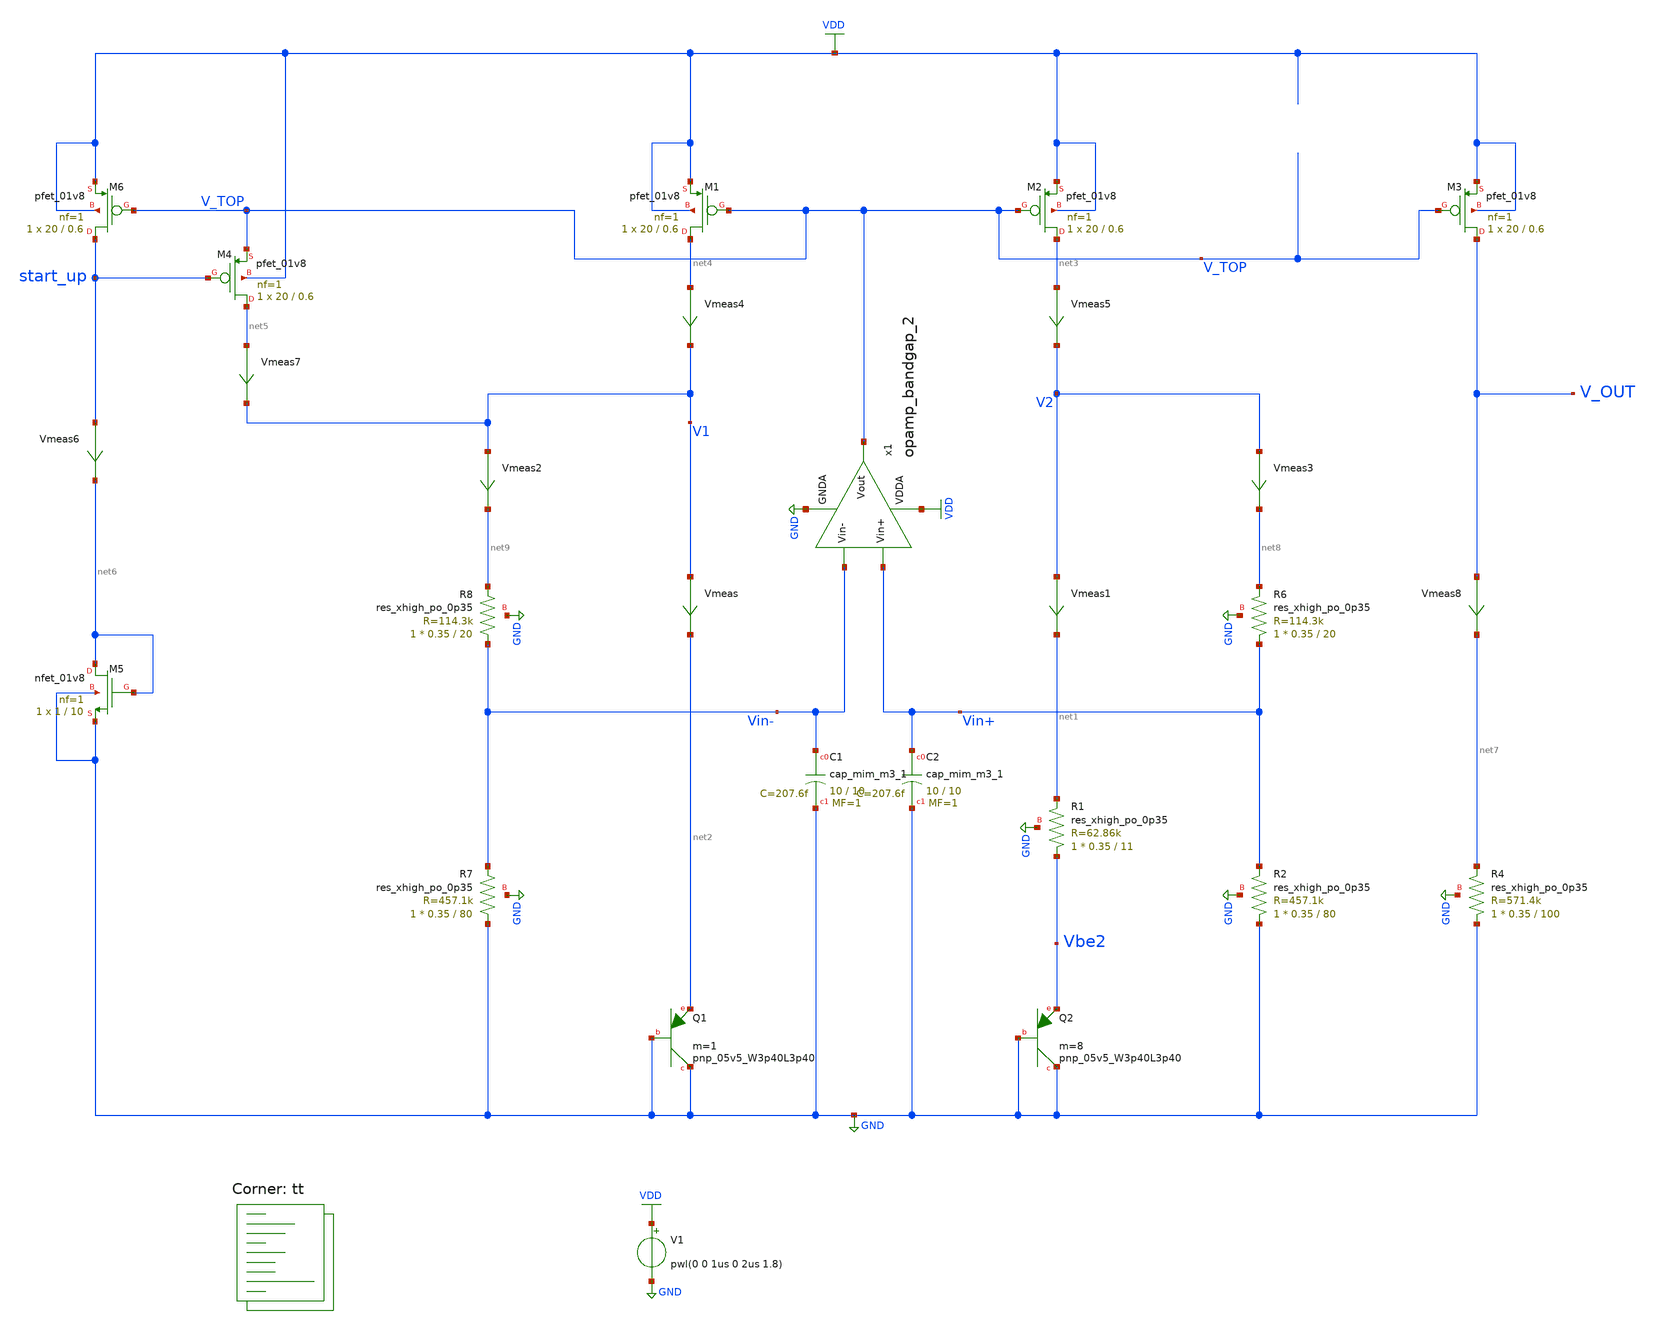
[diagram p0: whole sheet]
** sch_path: projects/bandgapref/xschem_ngspice/new_files/tb_low_voltage_BGR_9.sch
**.subckt tb_low_voltage_BGR_9
V1 VDD GND pwl(0 0 1us 0 2us 1.8)
XQ1 GND GND net2 sky130_fd_pr__pnp_05v5_W3p40L3p40 m=1
XQ2 GND GND Vbe2 sky130_fd_pr__pnp_05v5_W3p40L3p40 m=8
XM1 net4 V_TOP VDD VDD sky130_fd_pr__pfet_01v8 L=0.6 W=20 nf=1 ad='int((nf+1)/2) * W/nf * 0.29' as='int((nf+2)/2) * W/nf * 0.29'
+ pd='2*int((nf+1)/2) * (W/nf + 0.29)' ps='2*int((nf+2)/2) * (W/nf + 0.29)' nrd='0.29 / W' nrs='0.29 / W'
+ sa=0 sb=0 sd=0 mult=1 m=1
XM2 net3 V_TOP VDD VDD sky130_fd_pr__pfet_01v8 L=0.6 W=20 nf=1 ad='int((nf+1)/2) * W/nf * 0.29' as='int((nf+2)/2) * W/nf * 0.29'
+ pd='2*int((nf+1)/2) * (W/nf + 0.29)' ps='2*int((nf+2)/2) * (W/nf + 0.29)' nrd='0.29 / W' nrs='0.29 / W'
+ sa=0 sb=0 sd=0 mult=1 m=1
XM3 V_OUT V_TOP VDD VDD sky130_fd_pr__pfet_01v8 L=0.6 W=20 nf=1 ad='int((nf+1)/2) * W/nf * 0.29' as='int((nf+2)/2) * W/nf * 0.29'
+ pd='2*int((nf+1)/2) * (W/nf + 0.29)' ps='2*int((nf+2)/2) * (W/nf + 0.29)' nrd='0.29 / W' nrs='0.29 / W'
+ sa=0 sb=0 sd=0 mult=1 m=1
Vmeas V1 net2 0
.save i(vmeas)
Vmeas1 V2 net1 0
.save i(vmeas1)
Vmeas2 V1 net9 0
.save i(vmeas2)
XR1 Vbe2 net1 GND sky130_fd_pr__res_xhigh_po_0p35 L=11 mult=1 m=1
XR2 GND Vin+ GND sky130_fd_pr__res_xhigh_po_0p35 L=80 mult=1 m=1
XR4 GND net7 GND sky130_fd_pr__res_xhigh_po_0p35 L=100 mult=1 m=1
Vmeas3 V2 net8 0
.save i(vmeas3)
Vmeas4 net4 V1 0
.save i(vmeas4)
XM5 net6 net6 GND GND sky130_fd_pr__nfet_01v8 L=10 W=1 nf=1 ad='int((nf+1)/2) * W/nf * 0.29' as='int((nf+2)/2) * W/nf * 0.29'
+ pd='2*int((nf+1)/2) * (W/nf + 0.29)' ps='2*int((nf+2)/2) * (W/nf + 0.29)' nrd='0.29 / W' nrs='0.29 / W'
+ sa=0 sb=0 sd=0 mult=1 m=1
XM6 start_up V_TOP VDD VDD sky130_fd_pr__pfet_01v8 L=0.6 W=20 nf=1 ad='int((nf+1)/2) * W/nf * 0.29' as='int((nf+2)/2) * W/nf * 0.29'
+ pd='2*int((nf+1)/2) * (W/nf + 0.29)' ps='2*int((nf+2)/2) * (W/nf + 0.29)' nrd='0.29 / W' nrs='0.29 / W'
+ sa=0 sb=0 sd=0 mult=1 m=1
Vmeas5 net3 V2 0
.save i(vmeas5)
XM4 net5 start_up V_TOP VDD sky130_fd_pr__pfet_01v8 L=0.6 W=20 nf=1 ad='int((nf+1)/2) * W/nf * 0.29'
+ as='int((nf+2)/2) * W/nf * 0.29' pd='2*int((nf+1)/2) * (W/nf + 0.29)' ps='2*int((nf+2)/2) * (W/nf + 0.29)'
+ nrd='0.29 / W' nrs='0.29 / W' sa=0 sb=0 sd=0 mult=1 m=1
Vmeas7 net5 V1 0
.save i(vmeas7)
x1 VDD V_TOP Vin- Vin+ GND opamp_bandgap_2
XR6 Vin+ net8 GND sky130_fd_pr__res_xhigh_po_0p35 L=20 mult=1 m=1
XR7 GND Vin- GND sky130_fd_pr__res_xhigh_po_0p35 L=80 mult=1 m=1
Vmeas8 V_OUT net7 0
.save i(vmeas8)
XR8 Vin- net9 GND sky130_fd_pr__res_xhigh_po_0p35 L=20 mult=1 m=1
Vmeas6 start_up net6 0
.save i(vmeas6)
XC1 Vin- GND sky130_fd_pr__cap_mim_m3_1 W=10 L=10 MF=1 m=1
XC2 Vin+ GND sky130_fd_pr__cap_mim_m3_1 W=10 L=10 MF=1 m=1
**** begin user architecture code
.lib $::SKYWATER_MODELS/sky130.lib.spice tt



.option method=gear
.option wnflag=1
.option savecurrents
* .temp =140

.save @m.xm1.msky130_fd_pr__pfet_01v8[gm] @m.xm1.msky130_fd_pr__pfet_01v8[vth] @m.xm1.msky130_fd_pr__pfet_01v8[vgs] @m.xm1.msky130_fd_pr__pfet_01v8[vds] @m.xm2.msky130_fd_pr__pfet_01v8[gm] @m.xm2.msky130_fd_pr__pfet_01v8[vth] @m.xm2.msky130_fd_pr__pfet_01v8[vgs] @m.xm2.msky130_fd_pr__pfet_01v8[vds] @m.xm3.msky130_fd_pr__pfet_01v8[gm] @m.xm4.msky130_fd_pr__pfet_01v8[gm] @m.xm4.msky130_fd_pr__nfet_01v8[gm] @m.x1.xm1.msky130_fd_pr__nfet_01v8[gm] @m.x1.xm2.msky130_fd_pr__nfet_01v8[gm] @m.x1.xm3.msky130_fd_pr__nfet_01v8[gm] @m.x1.xm4.msky130_fd_pr__pfet_01v8[gm] @m.x1.xm5.msky130_fd_pr__pfet_01v8[gm] @m.x1.xm6.msky130_fd_pr__nfet_01v8[gm] @m.x1.xm7.msky130_fd_pr__pfet_01v8[gm] @m.x2.xm1.msky130_fd_pr__nfet_01v8[gm] @m.x2.xm2.msky130_fd_pr__nfet_01v8[gm] @m.x2.xm3.msky130_fd_pr__nfet_01v8[gm] @m.x2.xm4.msky130_fd_pr__pfet_01v8[gm] @m.x2.xm5.msky130_fd_pr__pfet_01v8[gm] @m.x2.xm6.msky130_fd_pr__pfet_01v8[gm] @m.x2.xm7.msky130_fd_pr__pfet_01v8[gm]

* .ic v(vin-) = 0.8
* .ic v(vin+) = 0.8
* .ic v(v_top) = 1.8

.control

    save all
    * dc temp -40 120 5 V1 1.6 2.0 0.05
    * dc V1 1.7 1.9 0.001 temp -40 120 40
    * dc V1 0.0 2.0 0.02 temp -40 120 40
    * dc V1 0 2.0 0.02
    tran 1ns 8us
    remzerovec
    * write tb_low_voltage_BGR_9.raw
    write tb_low_voltage_BGR_9_2.raw

.endc



**** end user architecture code
**.ends

* expanding   symbol:  opamp_bandgap_2.sym # of pins=5
** sym_path: projects/bandgapref/xschem_ngspice/new_files/opamp_bandgap_2.sym
** sch_path: projects/bandgapref/xschem_ngspice/new_files/opamp_bandgap_2.sch
.subckt opamp_bandgap_2 VDDA Vout Vin- Vin+ GNDA
*.ipin Vin+
*.opin Vout
*.ipin Vin-
*.ipin GNDA
*.ipin VDDA
XM1 V_p V_mirror GNDA GNDA sky130_fd_pr__nfet_01v8 L=10 W=10 nf=1 ad='int((nf+1)/2) * W/nf * 0.29' as='int((nf+2)/2) * W/nf * 0.29'
+ pd='2*int((nf+1)/2) * (W/nf + 0.29)' ps='2*int((nf+2)/2) * (W/nf + 0.29)' nrd='0.29 / W' nrs='0.29 / W'
+ sa=0 sb=0 sd=0 mult=1 m=1
XM2 V_mirror Vin- V_p GNDA sky130_fd_pr__nfet_01v8 L=1.2 W=10 nf=1 ad='int((nf+1)/2) * W/nf * 0.29' as='int((nf+2)/2) * W/nf * 0.29'
+ pd='2*int((nf+1)/2) * (W/nf + 0.29)' ps='2*int((nf+2)/2) * (W/nf + 0.29)' nrd='0.29 / W' nrs='0.29 / W'
+ sa=0 sb=0 sd=0 mult=1 m=1
XM3 1st_Vout Vin+ V_p GNDA sky130_fd_pr__nfet_01v8 L=1.2 W=10 nf=1 ad='int((nf+1)/2) * W/nf * 0.29' as='int((nf+2)/2) * W/nf * 0.29'
+ pd='2*int((nf+1)/2) * (W/nf + 0.29)' ps='2*int((nf+2)/2) * (W/nf + 0.29)' nrd='0.29 / W' nrs='0.29 / W'
+ sa=0 sb=0 sd=0 mult=1 m=1
XM4 V_mirror V_mirror VDDA VDDA sky130_fd_pr__pfet_01v8 L=1.2 W=20 nf=2 ad='int((nf+1)/2) * W/nf * 0.29'
+ as='int((nf+2)/2) * W/nf * 0.29' pd='2*int((nf+1)/2) * (W/nf + 0.29)' ps='2*int((nf+2)/2) * (W/nf + 0.29)'
+ nrd='0.29 / W' nrs='0.29 / W' sa=0 sb=0 sd=0 mult=1 m=1
XM5 1st_Vout V_mirror VDDA VDDA sky130_fd_pr__pfet_01v8 L=1.2 W=20 nf=2 ad='int((nf+1)/2) * W/nf * 0.29'
+ as='int((nf+2)/2) * W/nf * 0.29' pd='2*int((nf+1)/2) * (W/nf + 0.29)' ps='2*int((nf+2)/2) * (W/nf + 0.29)'
+ nrd='0.29 / W' nrs='0.29 / W' sa=0 sb=0 sd=0 mult=1 m=1
XM6 Vout V_mirror GNDA GNDA sky130_fd_pr__nfet_01v8 L=10 W=10 nf=1 ad='int((nf+1)/2) * W/nf * 0.29' as='int((nf+2)/2) * W/nf * 0.29'
+ pd='2*int((nf+1)/2) * (W/nf + 0.29)' ps='2*int((nf+2)/2) * (W/nf + 0.29)' nrd='0.29 / W' nrs='0.29 / W'
+ sa=0 sb=0 sd=0 mult=1 m=1
XM7 Vout 1st_Vout VDDA VDDA sky130_fd_pr__pfet_01v8 L=1.2 W=20 nf=2 ad='int((nf+1)/2) * W/nf * 0.29'
+ as='int((nf+2)/2) * W/nf * 0.29' pd='2*int((nf+1)/2) * (W/nf + 0.29)' ps='2*int((nf+2)/2) * (W/nf + 0.29)'
+ nrd='0.29 / W' nrs='0.29 / W' sa=0 sb=0 sd=0 mult=1 m=1
.ends

.GLOBAL GND
.GLOBAL VDD
.end
